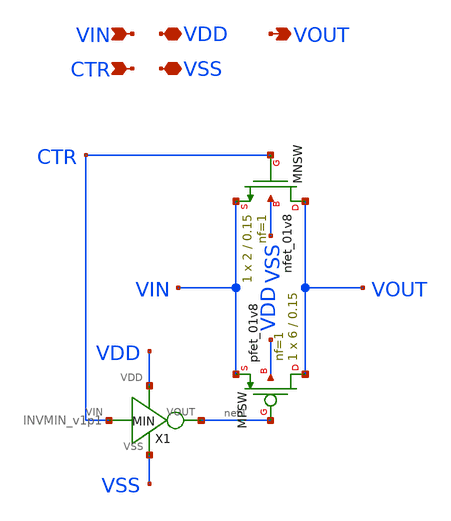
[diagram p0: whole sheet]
** sch_path: samples/cace-tests/SDC/xschem/PASSGATE_v1p2.sch
**.subckt PASSGATE_v1p2 VIN VDD VSS CTR VOUT
*.ipin VIN
*.iopin VDD
*.iopin VSS
*.ipin CTR
*.opin VOUT
XMNSW VOUT CTR VIN VSS sky130_fd_pr__nfet_01v8 L=0.15 W=2 nf=1 ad='int((nf+1)/2) * W/nf * 0.29' as='int((nf+2)/2) * W/nf * 0.29'
+ pd='2*int((nf+1)/2) * (W/nf + 0.29)' ps='2*int((nf+2)/2) * (W/nf + 0.29)' nrd='0.29 / W' nrs='0.29 / W'
+ sa=0 sb=0 sd=0 mult=1 m=1
XMPSW VOUT net1 VIN VDD sky130_fd_pr__pfet_01v8 L=0.15 W=6 nf=1 ad='int((nf+1)/2) * W/nf * 0.29' as='int((nf+2)/2) * W/nf * 0.29'
+ pd='2*int((nf+1)/2) * (W/nf + 0.29)' ps='2*int((nf+2)/2) * (W/nf + 0.29)' nrd='0.29 / W' nrs='0.29 / W'
+ sa=0 sb=0 sd=0 mult=1 m=1
X1 CTR net1 VDD VSS INVMIN_v1p1
**.ends

* expanding   symbol:  INVMIN_v1p1.sym # of pins=4
** sym_path: samples/cace-tests/SDC/xschem/INVMIN_v1p1.sym
** sch_path: samples/cace-tests/SDC/xschem/INVMIN_v1p1.sch
.subckt INVMIN_v1p1 VIN VOUT VDD VSS
*.ipin VIN
*.iopin VDD
*.iopin VSS
*.opin VOUT
XM1 VOUT VIN VSS VSS sky130_fd_pr__nfet_01v8 L=0.15 W=1 nf=1 ad='int((nf+1)/2) * W/nf * 0.29' as='int((nf+2)/2) * W/nf * 0.29'
+ pd='2*int((nf+1)/2) * (W/nf + 0.29)' ps='2*int((nf+2)/2) * (W/nf + 0.29)' nrd='0.29 / W' nrs='0.29 / W'
+ sa=0 sb=0 sd=0 mult=1 m=1
XM2 VOUT VIN VDD VDD sky130_fd_pr__pfet_01v8 L=0.15 W=1 nf=1 ad='int((nf+1)/2) * W/nf * 0.29' as='int((nf+2)/2) * W/nf * 0.29'
+ pd='2*int((nf+1)/2) * (W/nf + 0.29)' ps='2*int((nf+2)/2) * (W/nf + 0.29)' nrd='0.29 / W' nrs='0.29 / W'
+ sa=0 sb=0 sd=0 mult=1 m=1
.ends

.end
